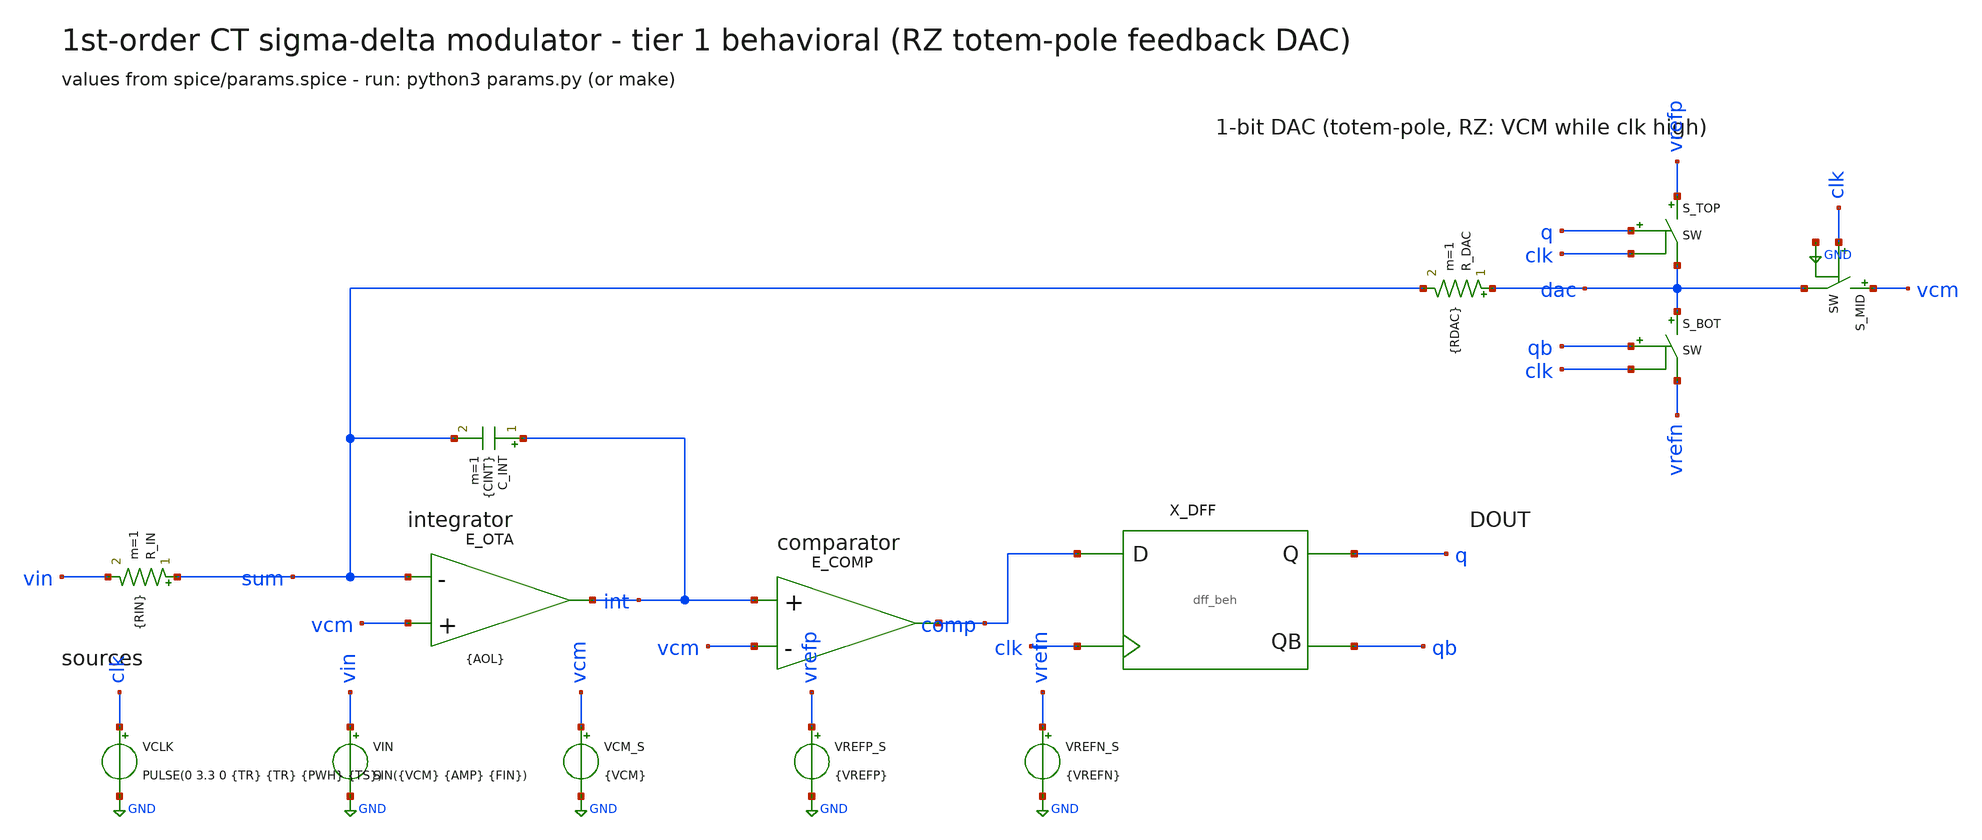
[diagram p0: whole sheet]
** sch_path: xschem/tier1_sdm.sch
**.subckt tier1_sdm
R_IN sum vin {RIN} m=1
E_OTA int GND vcm sum {AOL}
C_INT int sum {CINT} m=1
E_COMP comp GND VOL='{VCM}+1.6*tanh(2000*(v( int )-v( vcm )))'
X_DFF comp clk q qb dff_beh
S_TOP vrefp dac q clk SW
S_BOT dac vrefn qb clk SW
S_MID vcm dac clk GND SW
R_DAC dac sum {RDAC} m=1
VCLK clk GND PULSE(0 3.3 0 {TR} {TR} {PWH} {TS})
VIN vin GND SIN({VCM} {AMP} {FIN})
VCM_S vcm GND {VCM}
VREFP_S vrefp GND {VREFP}
VREFN_S vrefn GND {VREFN}
**** begin user architecture code

.include params.spice
.model SW sw vt=1.65 vh=0.1 ron=100 roff=1e9
* behavioral DFF: master/slave sample-and-hold of D at rising CLK edge
.subckt dff_beh D CLK Q QB
V_L vddl 0 3.3
S_M D m vddl CLK SW
C_M m 0 100f
S_S m qraw CLK 0 SW
C_Q qraw 0 100f
E_Q Q 0 VOL='1.65+1.65*tanh(20*(v(qraw)-1.65))'
E_QB QB 0 VOL='3.3-v(Q)'
.ends
.ic v(int)={VCM}
.tran {TSTEP} {TSTOP} uic
.control
run
wrdata tier1_out.csv v(q) v(clk) v(vin) v(int)
plot v(vin) v(int)
plot v(q) v(clk) v(dac) xlimit 0 2u
.endc


**** end user architecture code
**.ends
.GLOBAL GND
.end
